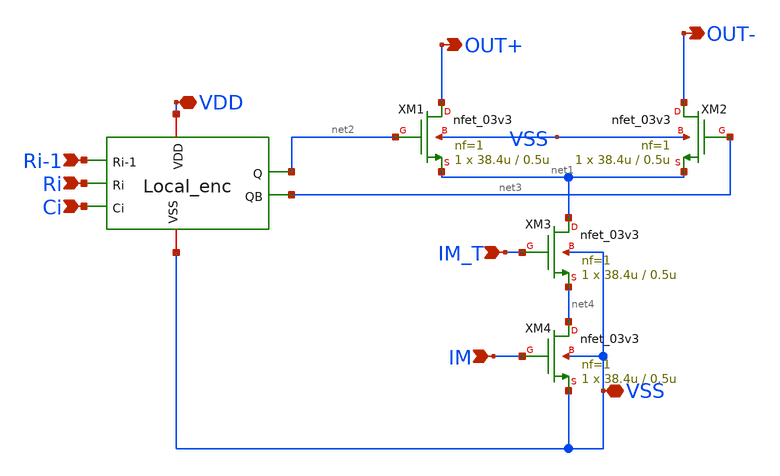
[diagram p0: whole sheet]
** sch_path: DAC_PAKISTAN_01/Pakistan1_Xschem/MSB_UNIT_CELL.sch
**.subckt MSB_UNIT_CELL VDD VSS Ri-1 Ri Ci IM_T IM OUT+ OUT-
*.iopin VDD
*.iopin VSS
*.ipin Ri-1
*.ipin Ri
*.ipin Ci
*.ipin IM_T
*.ipin IM
*.opin OUT+
*.opin OUT-
x1 VDD VSS Ri-1 Ri Ci net2 net3 Local_Enc
XM1 OUT+ net2 net1 VSS nfet_03v3 L=0.5u W=38.4u nf=1 ad='int((nf+1)/2) * W/nf * 0.18u' as='int((nf+2)/2) * W/nf * 0.18u'
+ pd='2*int((nf+1)/2) * (W/nf + 0.18u)' ps='2*int((nf+2)/2) * (W/nf + 0.18u)' nrd='0.18u / W' nrs='0.18u / W'
+ sa=0 sb=0 sd=0 m=1
XM2 OUT- net3 net1 VSS nfet_03v3 L=0.5u W=38.4u nf=1 ad='int((nf+1)/2) * W/nf * 0.18u' as='int((nf+2)/2) * W/nf * 0.18u'
+ pd='2*int((nf+1)/2) * (W/nf + 0.18u)' ps='2*int((nf+2)/2) * (W/nf + 0.18u)' nrd='0.18u / W' nrs='0.18u / W'
+ sa=0 sb=0 sd=0 m=1
XM3 net1 IM_T net4 VSS nfet_03v3 L=0.5u W=38.4u nf=1 ad='int((nf+1)/2) * W/nf * 0.18u' as='int((nf+2)/2) * W/nf * 0.18u'
+ pd='2*int((nf+1)/2) * (W/nf + 0.18u)' ps='2*int((nf+2)/2) * (W/nf + 0.18u)' nrd='0.18u / W' nrs='0.18u / W'
+ sa=0 sb=0 sd=0 m=1
XM4 net4 IM VSS VSS nfet_03v3 L=0.5u W=38.4u nf=1 ad='int((nf+1)/2) * W/nf * 0.18u' as='int((nf+2)/2) * W/nf * 0.18u'
+ pd='2*int((nf+1)/2) * (W/nf + 0.18u)' ps='2*int((nf+2)/2) * (W/nf + 0.18u)' nrd='0.18u / W' nrs='0.18u / W'
+ sa=0 sb=0 sd=0 m=1
**.ends
.end
